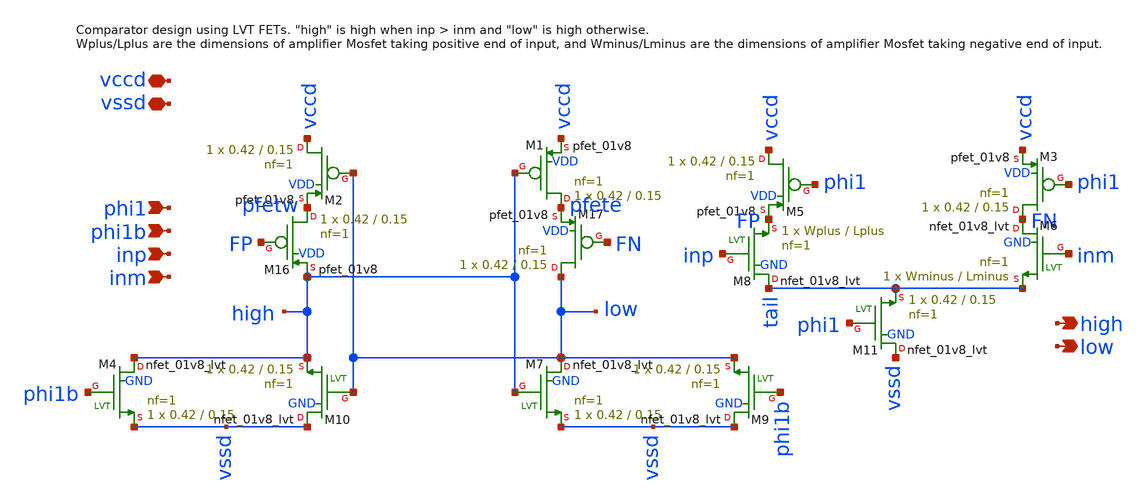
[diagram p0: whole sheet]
** sch_path: xschem/comparator_latest/comparator_single_tail.sch
**.subckt comparator_single_tail phi1 high phi1b inp inm low vccd vssd
*.ipin phi1
*.opin high
*.ipin phi1b
*.ipin inp
*.ipin inm
*.opin low
*.iopin vccd
*.iopin vssd
XM1 pfete high vccd VDD sky130_fd_pr__pfet_01v8 L=0.15 W=0.42 nf=1 ad='int((nf+1)/2) * W/nf * 0.29' as='int((nf+2)/2) * W/nf * 0.29'
+ pd='2*int((nf+1)/2) * (W/nf + 0.29)' ps='2*int((nf+2)/2) * (W/nf + 0.29)' nrd='0.29 / W' nrs='0.29 / W'
+ sa=0 sb=0 sd=0 mult=1 m=1
XM2 vccd low pfetw VDD sky130_fd_pr__pfet_01v8 L=0.15 W=0.42 nf=1 ad='int((nf+1)/2) * W/nf * 0.29' as='int((nf+2)/2) * W/nf * 0.29'
+ pd='2*int((nf+1)/2) * (W/nf + 0.29)' ps='2*int((nf+2)/2) * (W/nf + 0.29)' nrd='0.29 / W' nrs='0.29 / W'
+ sa=0 sb=0 sd=0 mult=1 m=1
XM16 pfetw FP high VDD sky130_fd_pr__pfet_01v8 L=0.15 W=0.42 nf=1 ad='int((nf+1)/2) * W/nf * 0.29' as='int((nf+2)/2) * W/nf * 0.29'
+ pd='2*int((nf+1)/2) * (W/nf + 0.29)' ps='2*int((nf+2)/2) * (W/nf + 0.29)' nrd='0.29 / W' nrs='0.29 / W'
+ sa=0 sb=0 sd=0 mult=1 m=1
XM17 low FN pfete VDD sky130_fd_pr__pfet_01v8 L=0.15 W=0.42 nf=1 ad='int((nf+1)/2) * W/nf * 0.29' as='int((nf+2)/2) * W/nf * 0.29'
+ pd='2*int((nf+1)/2) * (W/nf + 0.29)' ps='2*int((nf+2)/2) * (W/nf + 0.29)' nrd='0.29 / W' nrs='0.29 / W'
+ sa=0 sb=0 sd=0 mult=1 m=1
XM3 FN phi1 vccd VDD sky130_fd_pr__pfet_01v8 L=0.15 W=0.42 nf=1 ad='int((nf+1)/2) * W/nf * 0.29' as='int((nf+2)/2) * W/nf * 0.29'
+ pd='2*int((nf+1)/2) * (W/nf + 0.29)' ps='2*int((nf+2)/2) * (W/nf + 0.29)' nrd='0.29 / W' nrs='0.29 / W'
+ sa=0 sb=0 sd=0 mult=1 m=1
XM5 vccd phi1 FP VDD sky130_fd_pr__pfet_01v8 L=0.15 W=0.42 nf=1 ad='int((nf+1)/2) * W/nf * 0.29' as='int((nf+2)/2) * W/nf * 0.29'
+ pd='2*int((nf+1)/2) * (W/nf + 0.29)' ps='2*int((nf+2)/2) * (W/nf + 0.29)' nrd='0.29 / W' nrs='0.29 / W'
+ sa=0 sb=0 sd=0 mult=1 m=1
XM4 high phi1b vssd GND sky130_fd_pr__nfet_01v8_lvt L=0.15 W=0.42 nf=1 ad='int((nf+1)/2) * W/nf * 0.29'
+ as='int((nf+2)/2) * W/nf * 0.29' pd='2*int((nf+1)/2) * (W/nf + 0.29)' ps='2*int((nf+2)/2) * (W/nf + 0.29)'
+ nrd='0.29 / W' nrs='0.29 / W' sa=0 sb=0 sd=0 mult=1 m=1
XM7 low high vssd GND sky130_fd_pr__nfet_01v8_lvt L=0.15 W=0.42 nf=1 ad='int((nf+1)/2) * W/nf * 0.29'
+ as='int((nf+2)/2) * W/nf * 0.29' pd='2*int((nf+1)/2) * (W/nf + 0.29)' ps='2*int((nf+2)/2) * (W/nf + 0.29)'
+ nrd='0.29 / W' nrs='0.29 / W' sa=0 sb=0 sd=0 mult=1 m=1
XM8 tail inp FP GND sky130_fd_pr__nfet_01v8_lvt L=Lplus W=Wplus nf=1 ad='int((nf+1)/2) * W/nf * 0.29'
+ as='int((nf+2)/2) * W/nf * 0.29' pd='2*int((nf+1)/2) * (W/nf + 0.29)' ps='2*int((nf+2)/2) * (W/nf + 0.29)'
+ nrd='0.29 / W' nrs='0.29 / W' sa=0 sb=0 sd=0 mult=1 m=1
XM6 FN inm tail GND sky130_fd_pr__nfet_01v8_lvt L=Lminus W=Wminus nf=1 ad='int((nf+1)/2) * W/nf * 0.29'
+ as='int((nf+2)/2) * W/nf * 0.29' pd='2*int((nf+1)/2) * (W/nf + 0.29)' ps='2*int((nf+2)/2) * (W/nf + 0.29)'
+ nrd='0.29 / W' nrs='0.29 / W' sa=0 sb=0 sd=0 mult=1 m=1
XM9 vssd phi1b low GND sky130_fd_pr__nfet_01v8_lvt L=0.15 W=0.42 nf=1 ad='int((nf+1)/2) * W/nf * 0.29'
+ as='int((nf+2)/2) * W/nf * 0.29' pd='2*int((nf+1)/2) * (W/nf + 0.29)' ps='2*int((nf+2)/2) * (W/nf + 0.29)'
+ nrd='0.29 / W' nrs='0.29 / W' sa=0 sb=0 sd=0 mult=1 m=1
XM10 vssd low high GND sky130_fd_pr__nfet_01v8_lvt L=0.15 W=0.42 nf=1 ad='int((nf+1)/2) * W/nf * 0.29'
+ as='int((nf+2)/2) * W/nf * 0.29' pd='2*int((nf+1)/2) * (W/nf + 0.29)' ps='2*int((nf+2)/2) * (W/nf + 0.29)'
+ nrd='0.29 / W' nrs='0.29 / W' sa=0 sb=0 sd=0 mult=1 m=1
XM11 vssd phi1 tail GND sky130_fd_pr__nfet_01v8_lvt L=0.15 W=0.42 nf=1 ad='int((nf+1)/2) * W/nf * 0.29'
+ as='int((nf+2)/2) * W/nf * 0.29' pd='2*int((nf+1)/2) * (W/nf + 0.29)' ps='2*int((nf+2)/2) * (W/nf + 0.29)'
+ nrd='0.29 / W' nrs='0.29 / W' sa=0 sb=0 sd=0 mult=1 m=1
**.ends
.end
